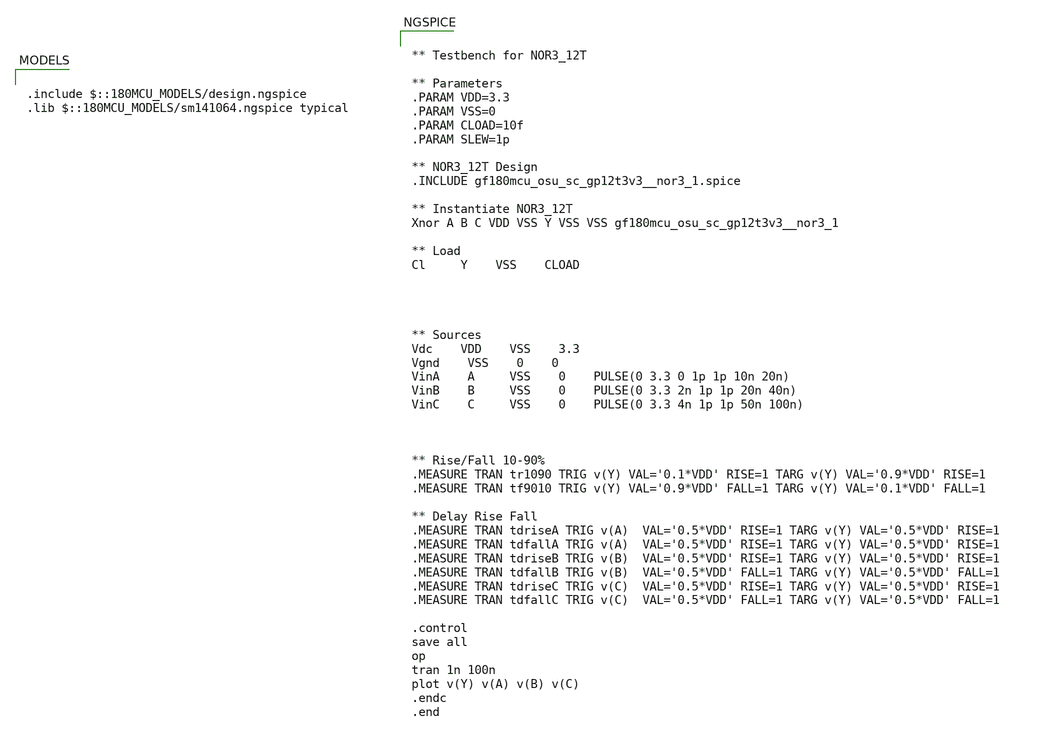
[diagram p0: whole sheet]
** sch_path: designs/libs/tb_digital/tb_nor3_12t/tb_gf180mcu_osu_sc_gp12t3v3__nor3_1.sch
**.subckt tb_gf180mcu_osu_sc_gp12t3v3__nor3_1
**** begin user architecture code


** Testbench for NOR3_12T

** Parameters
.PARAM VDD=3.3
.PARAM VSS=0
.PARAM CLOAD=10f
.PARAM SLEW=1p

** NOR3_12T Design
.INCLUDE gf180mcu_osu_sc_gp12t3v3__nor3_1.spice

** Instantiate NOR3_12T
Xnor A B C VDD VSS Y VSS VSS gf180mcu_osu_sc_gp12t3v3__nor3_1

** Load
Cl 	Y	VSS	CLOAD




** Sources
Vdc	VDD	VSS	3.3
Vgnd	VSS	0	0
VinA	A 	VSS	0	PULSE(0 3.3 0 1p 1p 10n 20n)
VinB	B 	VSS	0	PULSE(0 3.3 2n 1p 1p 20n 40n)
VinC	C 	VSS	0	PULSE(0 3.3 4n 1p 1p 50n 100n)



** Rise/Fall 10-90%
.MEASURE TRAN tr1090 TRIG v(Y) VAL='0.1*VDD' RISE=1 TARG v(Y) VAL='0.9*VDD' RISE=1
.MEASURE TRAN tf9010 TRIG v(Y) VAL='0.9*VDD' FALL=1 TARG v(Y) VAL='0.1*VDD' FALL=1

** Delay Rise Fall
.MEASURE TRAN tdriseA TRIG v(A)  VAL='0.5*VDD' RISE=1 TARG v(Y) VAL='0.5*VDD' RISE=1
.MEASURE TRAN tdfallA TRIG v(A)  VAL='0.5*VDD' RISE=1 TARG v(Y) VAL='0.5*VDD' RISE=1
.MEASURE TRAN tdriseB TRIG v(B)  VAL='0.5*VDD' RISE=1 TARG v(Y) VAL='0.5*VDD' RISE=1
.MEASURE TRAN tdfallB TRIG v(B)  VAL='0.5*VDD' FALL=1 TARG v(Y) VAL='0.5*VDD' FALL=1
.MEASURE TRAN tdriseC TRIG v(C)  VAL='0.5*VDD' RISE=1 TARG v(Y) VAL='0.5*VDD' RISE=1
.MEASURE TRAN tdfallC TRIG v(C)  VAL='0.5*VDD' FALL=1 TARG v(Y) VAL='0.5*VDD' FALL=1

.control
save all
op
tran 1n 100n
plot v(Y) v(A) v(B) v(C)
.endc
.end



.include $::180MCU_MODELS/design.ngspice
.lib $::180MCU_MODELS/sm141064.ngspice typical

**** end user architecture code
**.ends
.end
